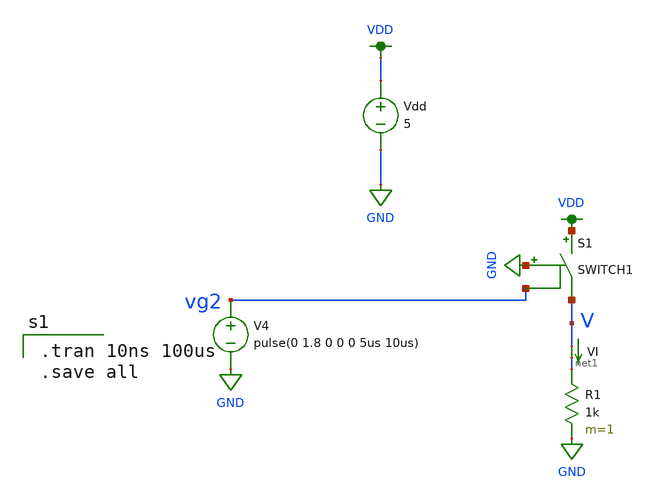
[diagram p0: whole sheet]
** sch_path: schematics/power_nfet_test.sch
**.subckt power_nfet_test
Vdd VDD GND 5
V4 vg2 GND pulse(0 1.8 0 0 0 5us 10us)
S1 VDD V GND vg2 SWITCH1
R1 net1 GND 1k m=1
VI V net1 0
.save i(vi)
**** begin user architecture code

.tran 10ns 100us
.save all


.option wnflag=1
.lib ~/skywater/skywater-pdk/libraries/sky130_fd_pr_ngspice/latest/models/sky130.lib.spice tt

**** end user architecture code
**.ends
.GLOBAL VDD
.GLOBAL GND
.end
